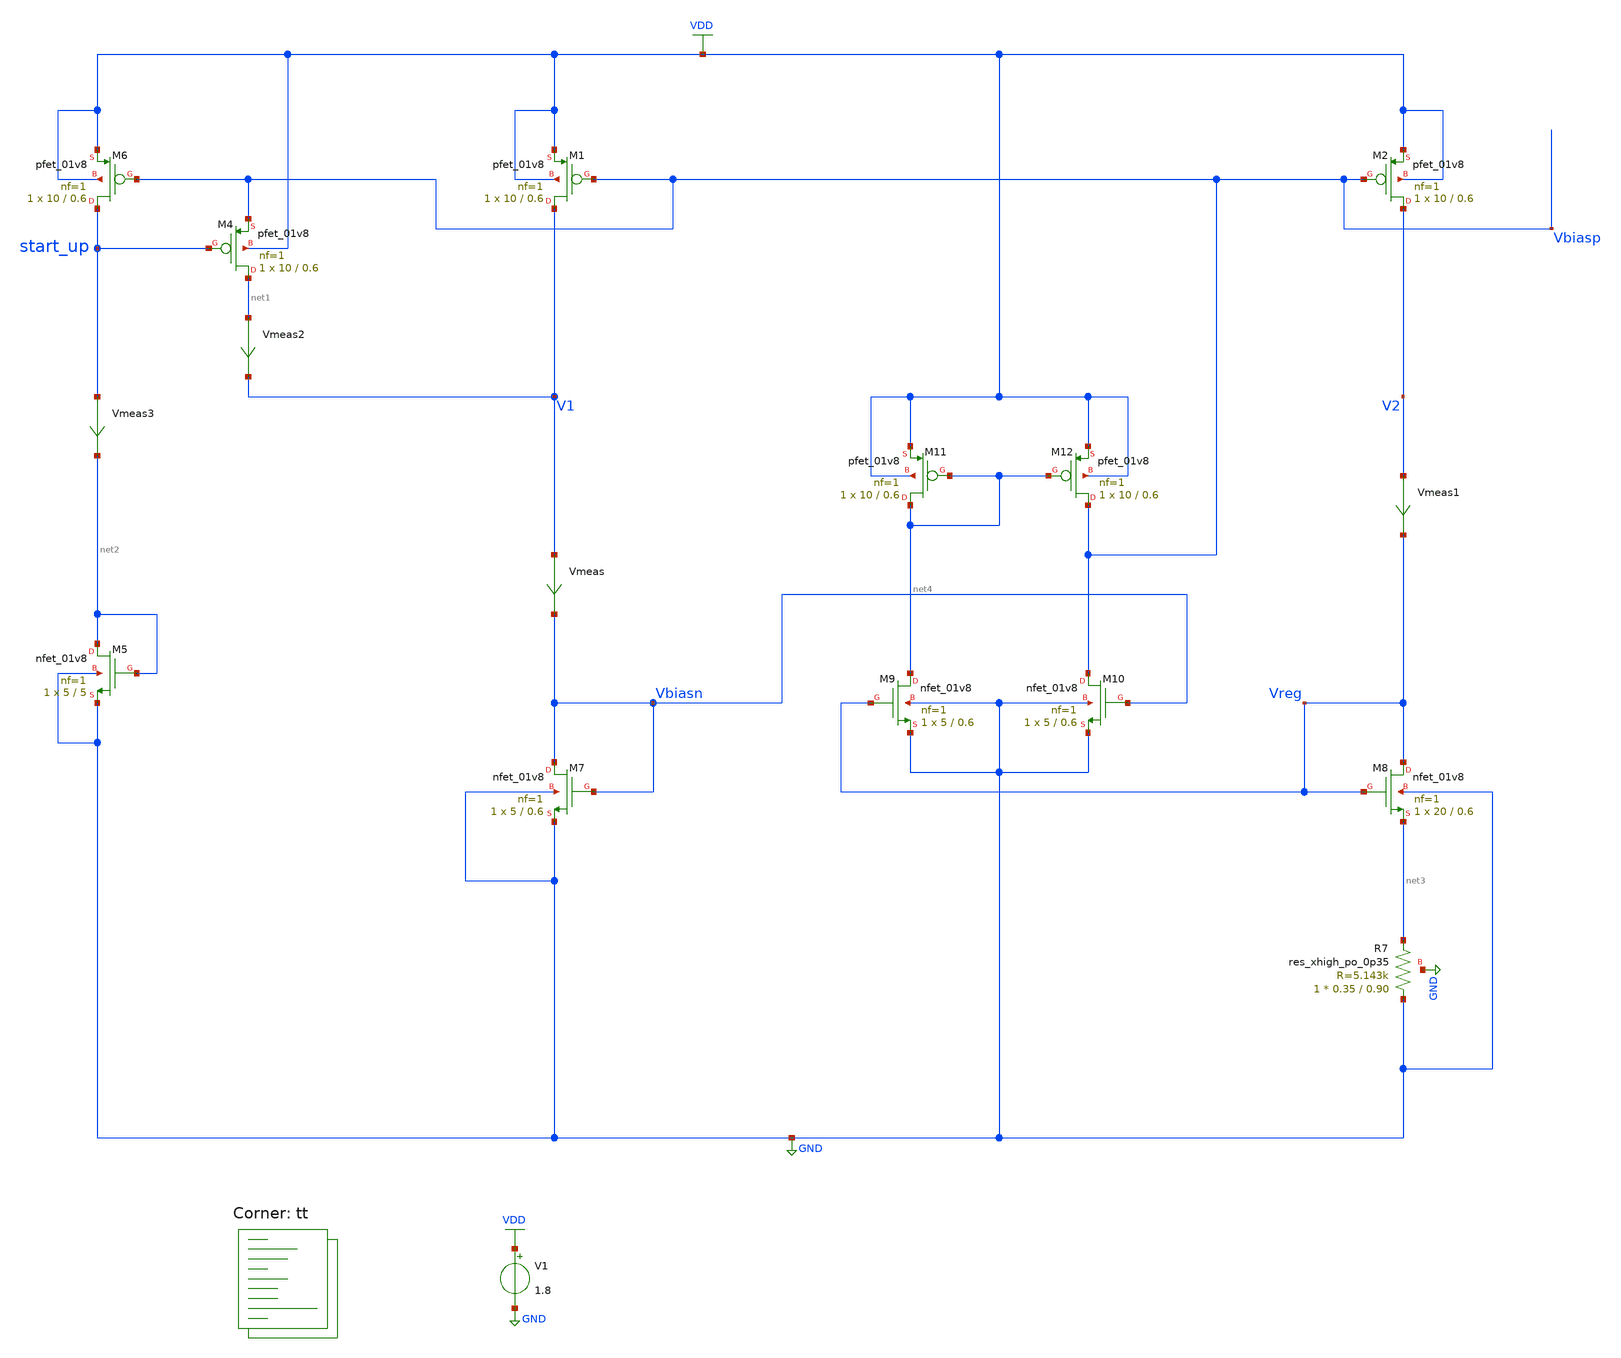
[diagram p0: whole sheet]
** sch_path: projects/bandgapref/xschem_ngspice/new_files/tb_low_voltage_BGR_7.sch
**.subckt tb_low_voltage_BGR_7
V1 VDD GND 1.8
XM1 V1 Vbiasp VDD VDD sky130_fd_pr__pfet_01v8 L=0.6 W=10 nf=1 ad='int((nf+1)/2) * W/nf * 0.29' as='int((nf+2)/2) * W/nf * 0.29'
+ pd='2*int((nf+1)/2) * (W/nf + 0.29)' ps='2*int((nf+2)/2) * (W/nf + 0.29)' nrd='0.29 / W' nrs='0.29 / W'
+ sa=0 sb=0 sd=0 mult=1 m=1
XM2 V2 Vbiasp VDD VDD sky130_fd_pr__pfet_01v8 L=0.6 W=10 nf=1 ad='int((nf+1)/2) * W/nf * 0.29' as='int((nf+2)/2) * W/nf * 0.29'
+ pd='2*int((nf+1)/2) * (W/nf + 0.29)' ps='2*int((nf+2)/2) * (W/nf + 0.29)' nrd='0.29 / W' nrs='0.29 / W'
+ sa=0 sb=0 sd=0 mult=1 m=1
Vmeas V1 Vbiasn 0
.save i(vmeas)
Vmeas1 V2 Vreg 0
.save i(vmeas1)
XM5 net2 net2 GND GND sky130_fd_pr__nfet_01v8 L=5 W=5 nf=1 ad='int((nf+1)/2) * W/nf * 0.29' as='int((nf+2)/2) * W/nf * 0.29'
+ pd='2*int((nf+1)/2) * (W/nf + 0.29)' ps='2*int((nf+2)/2) * (W/nf + 0.29)' nrd='0.29 / W' nrs='0.29 / W'
+ sa=0 sb=0 sd=0 mult=1 m=1
XM6 start_up Vbiasp VDD VDD sky130_fd_pr__pfet_01v8 L=0.6 W=10 nf=1 ad='int((nf+1)/2) * W/nf * 0.29'
+ as='int((nf+2)/2) * W/nf * 0.29' pd='2*int((nf+1)/2) * (W/nf + 0.29)' ps='2*int((nf+2)/2) * (W/nf + 0.29)'
+ nrd='0.29 / W' nrs='0.29 / W' sa=0 sb=0 sd=0 mult=1 m=1
XM4 net1 start_up Vbiasp VDD sky130_fd_pr__pfet_01v8 L=0.6 W=10 nf=1 ad='int((nf+1)/2) * W/nf * 0.29'
+ as='int((nf+2)/2) * W/nf * 0.29' pd='2*int((nf+1)/2) * (W/nf + 0.29)' ps='2*int((nf+2)/2) * (W/nf + 0.29)'
+ nrd='0.29 / W' nrs='0.29 / W' sa=0 sb=0 sd=0 mult=1 m=1
XM7 Vbiasn Vbiasn GND GND sky130_fd_pr__nfet_01v8 L=0.6 W=5 nf=1 ad='int((nf+1)/2) * W/nf * 0.29' as='int((nf+2)/2) * W/nf * 0.29'
+ pd='2*int((nf+1)/2) * (W/nf + 0.29)' ps='2*int((nf+2)/2) * (W/nf + 0.29)' nrd='0.29 / W' nrs='0.29 / W'
+ sa=0 sb=0 sd=0 mult=1 m=1
XM8 Vreg Vreg net3 GND sky130_fd_pr__nfet_01v8 L=0.6 W=20 nf=1 ad='int((nf+1)/2) * W/nf * 0.29' as='int((nf+2)/2) * W/nf * 0.29'
+ pd='2*int((nf+1)/2) * (W/nf + 0.29)' ps='2*int((nf+2)/2) * (W/nf + 0.29)' nrd='0.29 / W' nrs='0.29 / W'
+ sa=0 sb=0 sd=0 mult=1 m=1
Vmeas2 net1 V1 0
.save i(vmeas2)
Vmeas3 start_up net2 0
.save i(vmeas3)
XM9 net4 Vreg GND GND sky130_fd_pr__nfet_01v8 L=0.6 W=5 nf=1 ad='int((nf+1)/2) * W/nf * 0.29' as='int((nf+2)/2) * W/nf * 0.29'
+ pd='2*int((nf+1)/2) * (W/nf + 0.29)' ps='2*int((nf+2)/2) * (W/nf + 0.29)' nrd='0.29 / W' nrs='0.29 / W'
+ sa=0 sb=0 sd=0 mult=1 m=1
XM10 Vbiasp Vbiasn GND GND sky130_fd_pr__nfet_01v8 L=0.6 W=5 nf=1 ad='int((nf+1)/2) * W/nf * 0.29' as='int((nf+2)/2) * W/nf * 0.29'
+ pd='2*int((nf+1)/2) * (W/nf + 0.29)' ps='2*int((nf+2)/2) * (W/nf + 0.29)' nrd='0.29 / W' nrs='0.29 / W'
+ sa=0 sb=0 sd=0 mult=1 m=1
XM11 net4 net4 VDD VDD sky130_fd_pr__pfet_01v8 L=0.6 W=10 nf=1 ad='int((nf+1)/2) * W/nf * 0.29' as='int((nf+2)/2) * W/nf * 0.29'
+ pd='2*int((nf+1)/2) * (W/nf + 0.29)' ps='2*int((nf+2)/2) * (W/nf + 0.29)' nrd='0.29 / W' nrs='0.29 / W'
+ sa=0 sb=0 sd=0 mult=1 m=1
XM12 Vbiasp net4 VDD VDD sky130_fd_pr__pfet_01v8 L=0.6 W=10 nf=1 ad='int((nf+1)/2) * W/nf * 0.29' as='int((nf+2)/2) * W/nf * 0.29'
+ pd='2*int((nf+1)/2) * (W/nf + 0.29)' ps='2*int((nf+2)/2) * (W/nf + 0.29)' nrd='0.29 / W' nrs='0.29 / W'
+ sa=0 sb=0 sd=0 mult=1 m=1
XR7 GND net3 GND sky130_fd_pr__res_xhigh_po_0p35 L=0.90 mult=1 m=1
**** begin user architecture code
.lib $::SKYWATER_MODELS/sky130.lib.spice tt



.option method=gear
.option wnflag=1
.option savecurrents
* .temp =140

.save @m.xm1.msky130_fd_pr__pfet_01v8[gm] @m.xm1.msky130_fd_pr__pfet_01v8[vth] @m.xm1.msky130_fd_pr__pfet_01v8[vgs] @m.xm1.msky130_fd_pr__pfet_01v8[vds] @m.xm2.msky130_fd_pr__pfet_01v8[gm] @m.xm2.msky130_fd_pr__pfet_01v8[vth] @m.xm2.msky130_fd_pr__pfet_01v8[vgs] @m.xm2.msky130_fd_pr__pfet_01v8[vds] @m.xm3.msky130_fd_pr__pfet_01v8[gm] @m.xm4.msky130_fd_pr__pfet_01v8[gm] @m.xm4.msky130_fd_pr__nfet_01v8[gm] @m.x1.xm1.msky130_fd_pr__nfet_01v8[gm] @m.x1.xm2.msky130_fd_pr__nfet_01v8[gm] @m.x1.xm3.msky130_fd_pr__nfet_01v8[gm] @m.x1.xm4.msky130_fd_pr__pfet_01v8[gm] @m.x1.xm5.msky130_fd_pr__pfet_01v8[gm] @m.x1.xm6.msky130_fd_pr__nfet_01v8[gm] @m.x1.xm7.msky130_fd_pr__pfet_01v8[gm] @m.x2.xm1.msky130_fd_pr__nfet_01v8[gm] @m.x2.xm2.msky130_fd_pr__nfet_01v8[gm] @m.x2.xm3.msky130_fd_pr__nfet_01v8[gm] @m.x2.xm4.msky130_fd_pr__pfet_01v8[gm] @m.x2.xm5.msky130_fd_pr__pfet_01v8[gm] @m.x2.xm6.msky130_fd_pr__pfet_01v8[gm] @m.x2.xm7.msky130_fd_pr__pfet_01v8[gm]

* .ic v(vin-) = 0.8
* .ic v(vin+) = 0.8
* .ic v(v_top) = 1.8

.control

  * let start_vdd = 0.3
  * let stop_vdd = 1.8
  * let delta_vdd = 0.3
  * let w_act = start_vdd
  * while w_act le stop_vdd
    * echo $&w_act
    * alter V1 = w_act
    * echo v[vdd]
    * alter @V1[pwl] = [ 0 0 1us 0 2us $&w_act ]
    * reset
    save all
    * run
    * dc temp -40 120 5 V1 1.6 2.0 0.05
    * dc V1 1.7 1.9 0.001 temp -40 120 40
    * dc V1 0 2.0 0.01 temp -40 120 40
    dc V1 0 2.0 0.01
    * tran 1ns 8us
    remzerovec
    write tb_low_voltage_BGR_7.raw
    * let w_act = w_act + delta_vdd
    set appendwrite
  * end

.endc



**** end user architecture code
**.ends
.GLOBAL GND
.GLOBAL VDD
.end
